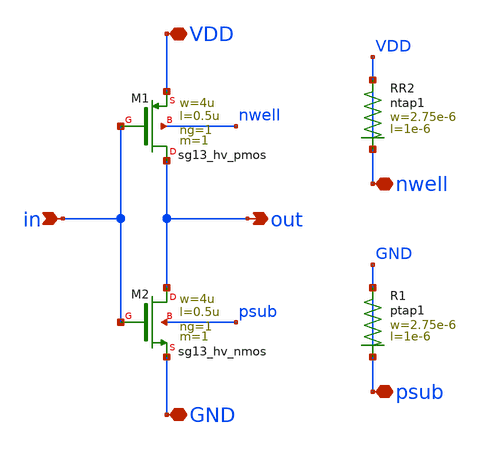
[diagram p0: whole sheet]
** sch_path: xschem/inv_BK.sch
**.subckt inv_BK in GND out VDD nwell psub
*.ipin in
*.iopin GND
*.opin out
*.iopin VDD
*.iopin nwell
*.iopin psub
XM1 out in VDD nwell sg13_hv_pmos w=4u l=0.5u ng=1 m=1 mm_ok=1
XM2 out in GND psub sg13_hv_nmos w=4u l=0.5u ng=1 m=1 mm_ok=1
XR1 psub psub ptap1 R=95.61 w=2.75e-6 l=1e-6
XR2 nwell nwell ntap1 R=95.61 w=2.75e-6 l=1e-6
**.ends
.end
